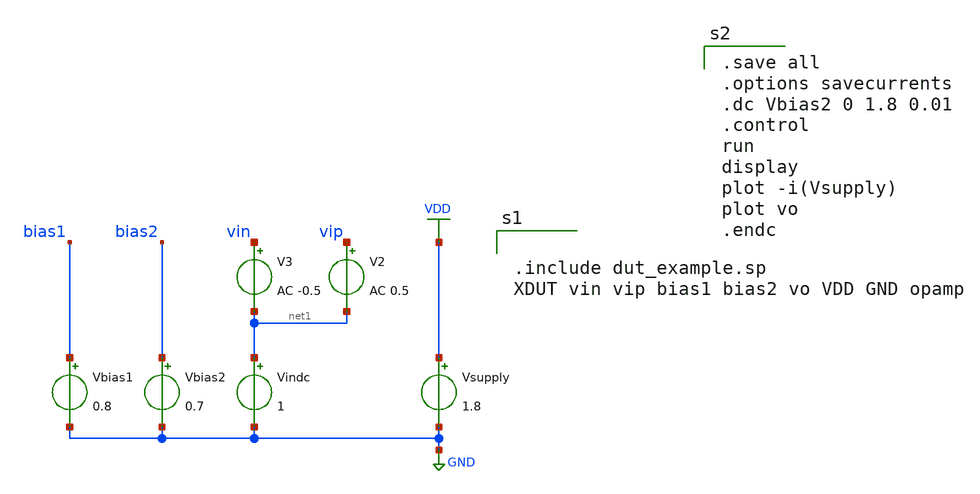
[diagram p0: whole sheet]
** sch_path: SKY130/opamp_perf_eval/02_s2bias.sch
**.subckt 02_s2bias
Vsupply VDD GND 1.8
V2 vip net1 AC 0.5
V3 vin net1 AC -0.5
Vbias2 bias2 GND 0.7
Vbias1 bias1 GND 0.8
Vindc net1 GND 1
**** begin user architecture code


.include dut_example.sp
XDUT vin vip bias1 bias2 vo VDD GND opamp


.lib $::SKYWATER_MODELS/sky130.lib.spice tt
.include $::PDKPATH/libs.ref/sky130_fd_sc_hvl/spice/sky130_fd_sc_hvl.spice

.save all
.options savecurrents
.dc Vbias2 0 1.8 0.01
.control
run
display
plot -i(Vsupply)
plot vo
.endc


**** end user architecture code
**.ends
.GLOBAL GND
.GLOBAL VDD
.end
